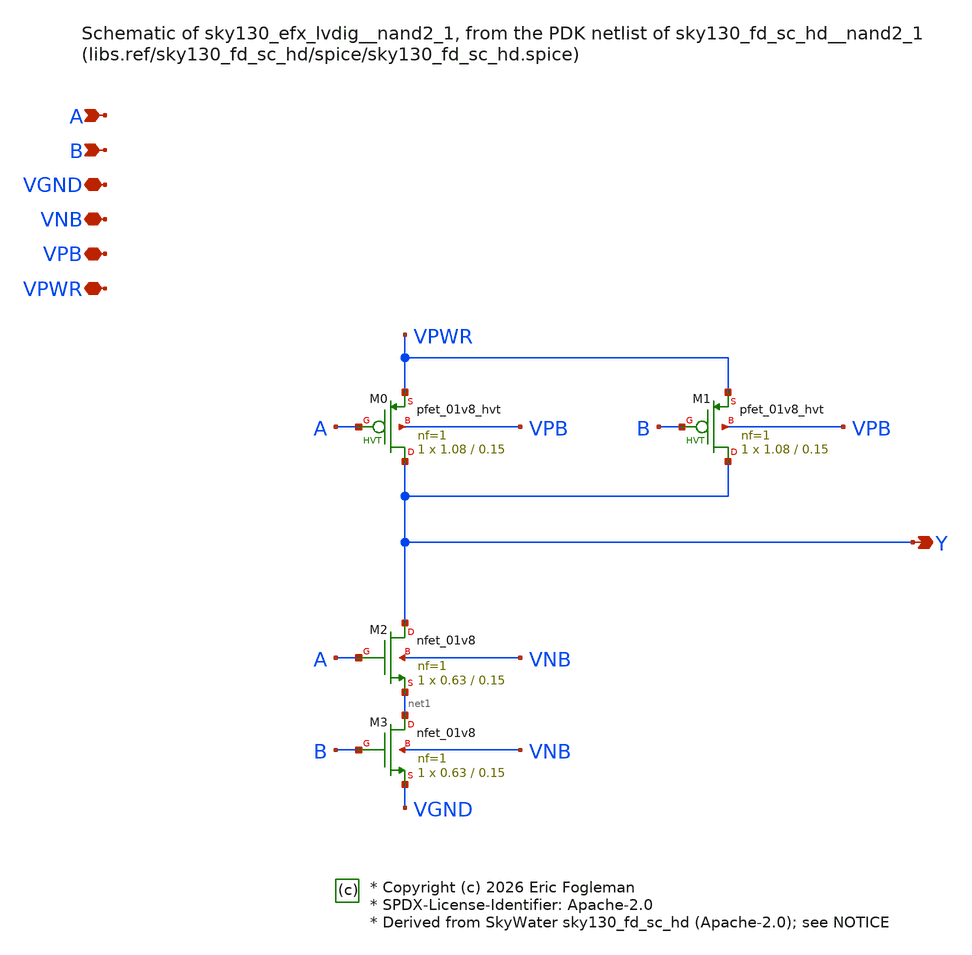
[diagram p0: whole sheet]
** sch_path: xschem/sky130_efx_lvdig__nand2_1.sch

* Copyright (c) 2026 Eric Fogleman
* SPDX-License-Identifier: Apache-2.0
* Derived from SkyWater sky130_fd_sc_hd (Apache-2.0); see NOTICE

**.subckt sky130_efx_lvdig__nand2_1 Y A B VGND VNB VPB VPWR
*.opin Y
*.ipin A
*.ipin B
*.iopin VGND
*.iopin VNB
*.iopin VPB
*.iopin VPWR
XM0 Y A VPWR VPB sky130_fd_pr__pfet_01v8_hvt L=0.15 W=1.08 nf=1 ad='int((1 + 1)/2) * 1.08 / 1 * 0.29'
+ as='int((1 + 2)/2) * 1.08 / 1 * 0.29' pd='2*int((1 + 1)/2) * (1.08 / 1 + 0.29)' ps='2*int((1 + 2)/2) * (1.08 / 1 + 0.29)'
+ nrd='0.29 / 1.08 ' nrs='0.29 / 1.08 ' sa=0 sb=0 sd=0 mult=1 m=1
XM1 Y B VPWR VPB sky130_fd_pr__pfet_01v8_hvt L=0.15 W=1.08 nf=1 ad='int((1 + 1)/2) * 1.08 / 1 * 0.29'
+ as='int((1 + 2)/2) * 1.08 / 1 * 0.29' pd='2*int((1 + 1)/2) * (1.08 / 1 + 0.29)' ps='2*int((1 + 2)/2) * (1.08 / 1 + 0.29)'
+ nrd='0.29 / 1.08 ' nrs='0.29 / 1.08 ' sa=0 sb=0 sd=0 mult=1 m=1
XM2 Y A net1 VNB sky130_fd_pr__nfet_01v8 L=0.15 W=0.63 nf=1 ad='int((1 + 1)/2) * 0.63 / 1 * 0.29' as='int((1 + 2)/2) * 0.63 / 1 * 0.29'
+ pd='2*int((1 + 1)/2) * (0.63 / 1 + 0.29)' ps='2*int((1 + 2)/2) * (0.63 / 1 + 0.29)' nrd='0.29 / 0.63 '
+ nrs='0.29 / 0.63 ' sa=0 sb=0 sd=0 mult=1 m=1
XM3 net1 B VGND VNB sky130_fd_pr__nfet_01v8 L=0.15 W=0.63 nf=1 ad='int((1 + 1)/2) * 0.63 / 1 * 0.29'
+ as='int((1 + 2)/2) * 0.63 / 1 * 0.29' pd='2*int((1 + 1)/2) * (0.63 / 1 + 0.29)' ps='2*int((1 + 2)/2) * (0.63 / 1 + 0.29)'
+ nrd='0.29 / 0.63 ' nrs='0.29 / 0.63 ' sa=0 sb=0 sd=0 mult=1 m=1
**.ends
.end
